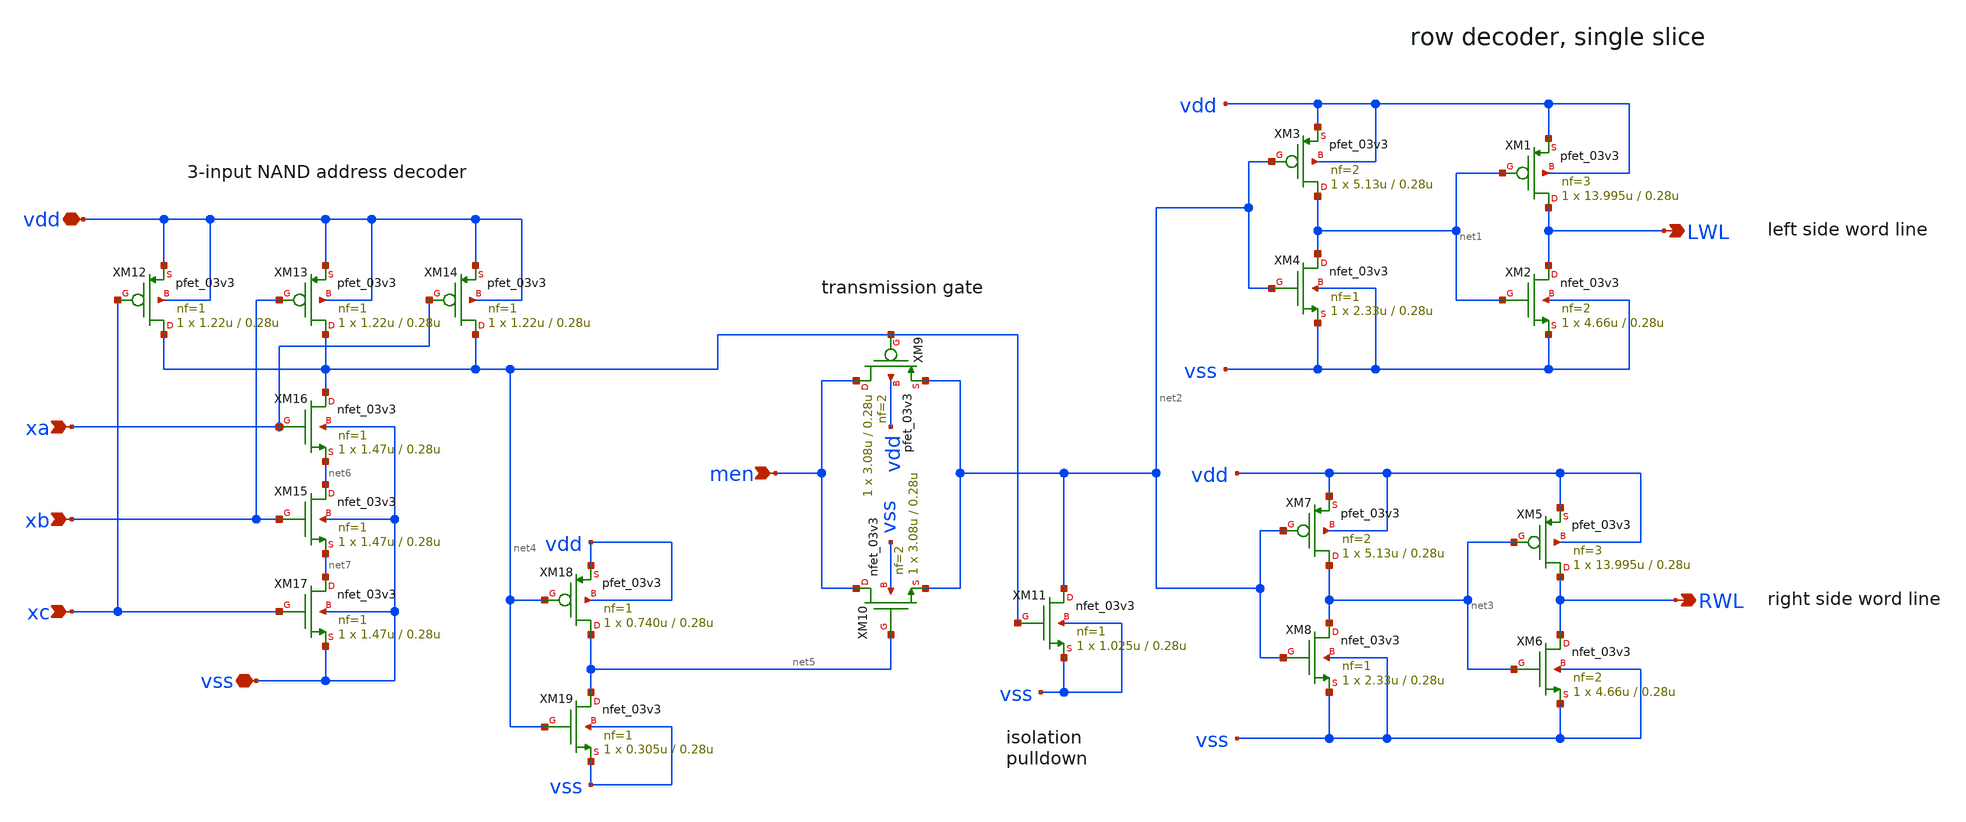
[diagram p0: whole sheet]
** sch_path: cells/gf180mcu_ocd_ip_sram__sram512x8m8wm1/xschem/xdec_3v512x8m81.sch
**.subckt xdec_3v512x8m81 xc xb xa vdd vss men LWL RWL
*.ipin xc
*.ipin xb
*.ipin xa
*.iopin vdd
*.iopin vss
*.ipin men
*.opin LWL
*.opin RWL
XM1 LWL net1 vdd vdd pfet_03v3 L=0.28u W=13.995u nf=3 ad='int((nf+1)/2) * W/nf * 0.18u' as='int((nf+2)/2) * W/nf * 0.18u'
+ pd='2*int((nf+1)/2) * (W/nf + 0.18u)' ps='2*int((nf+2)/2) * (W/nf + 0.18u)' nrd='0.18u / W' nrs='0.18u / W'
+ sa=0 sb=0 sd=0 m=1
XM2 LWL net1 vss vss nfet_03v3 L=0.28u W=4.66u nf=2 ad='int((nf+1)/2) * W/nf * 0.18u' as='int((nf+2)/2) * W/nf * 0.18u'
+ pd='2*int((nf+1)/2) * (W/nf + 0.18u)' ps='2*int((nf+2)/2) * (W/nf + 0.18u)' nrd='0.18u / W' nrs='0.18u / W'
+ sa=0 sb=0 sd=0 m=1
XM3 net1 net2 vdd vdd pfet_03v3 L=0.28u W=5.13u nf=2 ad='int((nf+1)/2) * W/nf * 0.18u' as='int((nf+2)/2) * W/nf * 0.18u'
+ pd='2*int((nf+1)/2) * (W/nf + 0.18u)' ps='2*int((nf+2)/2) * (W/nf + 0.18u)' nrd='0.18u / W' nrs='0.18u / W'
+ sa=0 sb=0 sd=0 m=1
XM4 net1 net2 vss vss nfet_03v3 L=0.28u W=2.33u nf=1 ad='int((nf+1)/2) * W/nf * 0.18u' as='int((nf+2)/2) * W/nf * 0.18u'
+ pd='2*int((nf+1)/2) * (W/nf + 0.18u)' ps='2*int((nf+2)/2) * (W/nf + 0.18u)' nrd='0.18u / W' nrs='0.18u / W'
+ sa=0 sb=0 sd=0 m=1
XM5 RWL net3 vdd vdd pfet_03v3 L=0.28u W=13.995u nf=3 ad='int((nf+1)/2) * W/nf * 0.18u' as='int((nf+2)/2) * W/nf * 0.18u'
+ pd='2*int((nf+1)/2) * (W/nf + 0.18u)' ps='2*int((nf+2)/2) * (W/nf + 0.18u)' nrd='0.18u / W' nrs='0.18u / W'
+ sa=0 sb=0 sd=0 m=1
XM6 RWL net3 vss vss nfet_03v3 L=0.28u W=4.66u nf=2 ad='int((nf+1)/2) * W/nf * 0.18u' as='int((nf+2)/2) * W/nf * 0.18u'
+ pd='2*int((nf+1)/2) * (W/nf + 0.18u)' ps='2*int((nf+2)/2) * (W/nf + 0.18u)' nrd='0.18u / W' nrs='0.18u / W'
+ sa=0 sb=0 sd=0 m=1
XM7 net3 net2 vdd vdd pfet_03v3 L=0.28u W=5.13u nf=2 ad='int((nf+1)/2) * W/nf * 0.18u' as='int((nf+2)/2) * W/nf * 0.18u'
+ pd='2*int((nf+1)/2) * (W/nf + 0.18u)' ps='2*int((nf+2)/2) * (W/nf + 0.18u)' nrd='0.18u / W' nrs='0.18u / W'
+ sa=0 sb=0 sd=0 m=1
XM8 net3 net2 vss vss nfet_03v3 L=0.28u W=2.33u nf=1 ad='int((nf+1)/2) * W/nf * 0.18u' as='int((nf+2)/2) * W/nf * 0.18u'
+ pd='2*int((nf+1)/2) * (W/nf + 0.18u)' ps='2*int((nf+2)/2) * (W/nf + 0.18u)' nrd='0.18u / W' nrs='0.18u / W'
+ sa=0 sb=0 sd=0 m=1
XM9 men net4 net2 vdd pfet_03v3 L=0.28u W=3.08u nf=2 ad='int((nf+1)/2) * W/nf * 0.18u' as='int((nf+2)/2) * W/nf * 0.18u'
+ pd='2*int((nf+1)/2) * (W/nf + 0.18u)' ps='2*int((nf+2)/2) * (W/nf + 0.18u)' nrd='0.18u / W' nrs='0.18u / W'
+ sa=0 sb=0 sd=0 m=1
XM10 men net5 net2 vss nfet_03v3 L=0.28u W=3.08u nf=2 ad='int((nf+1)/2) * W/nf * 0.18u' as='int((nf+2)/2) * W/nf * 0.18u'
+ pd='2*int((nf+1)/2) * (W/nf + 0.18u)' ps='2*int((nf+2)/2) * (W/nf + 0.18u)' nrd='0.18u / W' nrs='0.18u / W'
+ sa=0 sb=0 sd=0 m=1
XM11 net2 net4 vss vss nfet_03v3 L=0.28u W=1.025u nf=1 ad='int((nf+1)/2) * W/nf * 0.18u' as='int((nf+2)/2) * W/nf * 0.18u'
+ pd='2*int((nf+1)/2) * (W/nf + 0.18u)' ps='2*int((nf+2)/2) * (W/nf + 0.18u)' nrd='0.18u / W' nrs='0.18u / W'
+ sa=0 sb=0 sd=0 m=1
XM12 net4 xc vdd vdd pfet_03v3 L=0.28u W=1.22u nf=1 ad='int((nf+1)/2) * W/nf * 0.18u' as='int((nf+2)/2) * W/nf * 0.18u'
+ pd='2*int((nf+1)/2) * (W/nf + 0.18u)' ps='2*int((nf+2)/2) * (W/nf + 0.18u)' nrd='0.18u / W' nrs='0.18u / W'
+ sa=0 sb=0 sd=0 m=1
XM13 net4 xb vdd vdd pfet_03v3 L=0.28u W=1.22u nf=1 ad='int((nf+1)/2) * W/nf * 0.18u' as='int((nf+2)/2) * W/nf * 0.18u'
+ pd='2*int((nf+1)/2) * (W/nf + 0.18u)' ps='2*int((nf+2)/2) * (W/nf + 0.18u)' nrd='0.18u / W' nrs='0.18u / W'
+ sa=0 sb=0 sd=0 m=1
XM14 net4 xa vdd vdd pfet_03v3 L=0.28u W=1.22u nf=1 ad='int((nf+1)/2) * W/nf * 0.18u' as='int((nf+2)/2) * W/nf * 0.18u'
+ pd='2*int((nf+1)/2) * (W/nf + 0.18u)' ps='2*int((nf+2)/2) * (W/nf + 0.18u)' nrd='0.18u / W' nrs='0.18u / W'
+ sa=0 sb=0 sd=0 m=1
XM17 net7 xc vss vss nfet_03v3 L=0.28u W=1.47u nf=1 ad='int((nf+1)/2) * W/nf * 0.18u' as='int((nf+2)/2) * W/nf * 0.18u'
+ pd='2*int((nf+1)/2) * (W/nf + 0.18u)' ps='2*int((nf+2)/2) * (W/nf + 0.18u)' nrd='0.18u / W' nrs='0.18u / W'
+ sa=0 sb=0 sd=0 m=1
XM18 net5 net4 vdd vdd pfet_03v3 L=0.28u W=0.740u nf=1 ad='int((nf+1)/2) * W/nf * 0.18u' as='int((nf+2)/2) * W/nf * 0.18u'
+ pd='2*int((nf+1)/2) * (W/nf + 0.18u)' ps='2*int((nf+2)/2) * (W/nf + 0.18u)' nrd='0.18u / W' nrs='0.18u / W'
+ sa=0 sb=0 sd=0 m=1
XM19 net5 net4 vss vss nfet_03v3 L=0.28u W=0.305u nf=1 ad='int((nf+1)/2) * W/nf * 0.18u' as='int((nf+2)/2) * W/nf * 0.18u'
+ pd='2*int((nf+1)/2) * (W/nf + 0.18u)' ps='2*int((nf+2)/2) * (W/nf + 0.18u)' nrd='0.18u / W' nrs='0.18u / W'
+ sa=0 sb=0 sd=0 m=1
XM15 net6 xb net7 vss nfet_03v3 L=0.28u W=1.47u nf=1 ad='int((nf+1)/2) * W/nf * 0.18u' as='int((nf+2)/2) * W/nf * 0.18u'
+ pd='2*int((nf+1)/2) * (W/nf + 0.18u)' ps='2*int((nf+2)/2) * (W/nf + 0.18u)' nrd='0.18u / W' nrs='0.18u / W'
+ sa=0 sb=0 sd=0 m=1
XM16 net4 xa net6 vss nfet_03v3 L=0.28u W=1.47u nf=1 ad='int((nf+1)/2) * W/nf * 0.18u' as='int((nf+2)/2) * W/nf * 0.18u'
+ pd='2*int((nf+1)/2) * (W/nf + 0.18u)' ps='2*int((nf+2)/2) * (W/nf + 0.18u)' nrd='0.18u / W' nrs='0.18u / W'
+ sa=0 sb=0 sd=0 m=1
**.ends
.end
